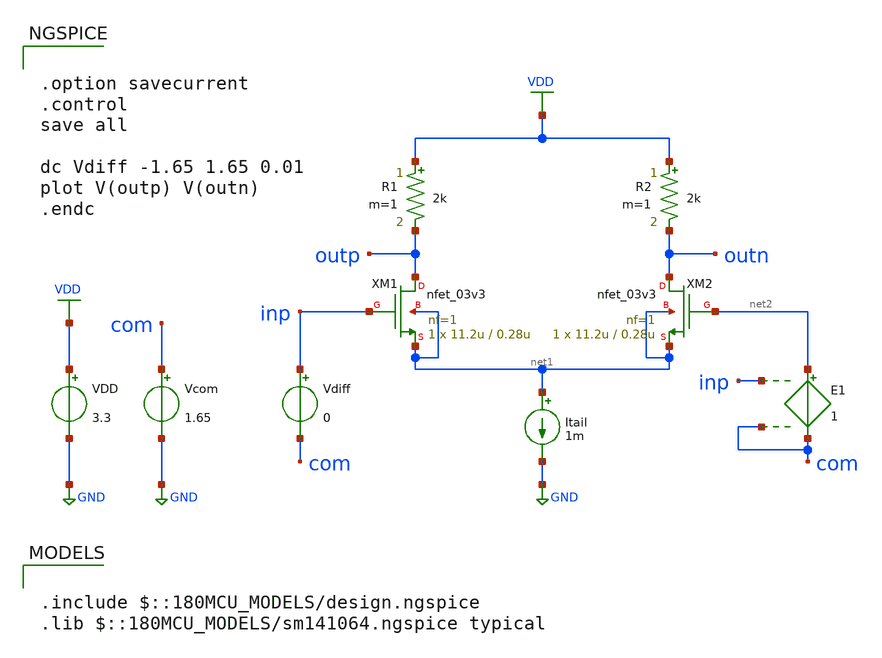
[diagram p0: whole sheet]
** sch_path: fifty_nifty/08_diff_dc2.sch
**.subckt 08_diff_dc2
XM1 outp inp net1 net1 nfet_03v3 L=0.28u W=11.2u nf=1 ad='int((nf+1)/2) * W/nf * 0.18u' as='int((nf+2)/2) * W/nf * 0.18u'
+ pd='2*int((nf+1)/2) * (W/nf + 0.18u)' ps='2*int((nf+2)/2) * (W/nf + 0.18u)' nrd='0.18u / W' nrs='0.18u / W'
+ sa=0 sb=0 sd=0 m=1
VDD VDD GND 3.3
XM2 outn net2 net1 net1 nfet_03v3 L=0.28u W=11.2u nf=1 ad='int((nf+1)/2) * W/nf * 0.18u' as='int((nf+2)/2) * W/nf * 0.18u'
+ pd='2*int((nf+1)/2) * (W/nf + 0.18u)' ps='2*int((nf+2)/2) * (W/nf + 0.18u)' nrd='0.18u / W' nrs='0.18u / W'
+ sa=0 sb=0 sd=0 m=1
Itail net1 GND 1m
Vdiff inp com 0
R1 VDD outp 2k m=1
R2 VDD outn 2k m=1
Vcom com GND 1.65
E1 net2 com inp com 1
**** begin user architecture code

.option savecurrent
.control
save all

dc Vdiff -1.65 1.65 0.01
plot V(outp) V(outn)
.endc


.include $::180MCU_MODELS/design.ngspice
.lib $::180MCU_MODELS/sm141064.ngspice typical

**** end user architecture code
**.ends
.GLOBAL GND
.GLOBAL VDD
.end
